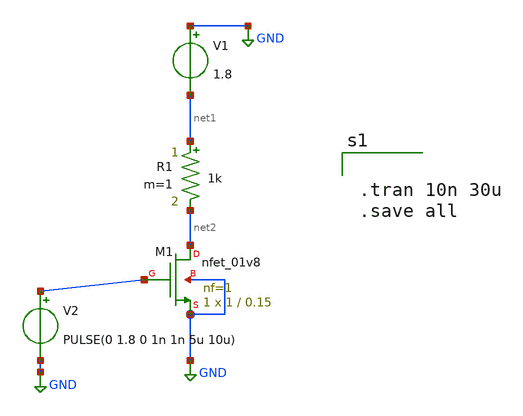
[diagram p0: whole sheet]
** sch_path: MOSFET_as_Switch/untitled.sch
**.subckt untitled
V1 GND net1 1.8
R1 net1 net2 1k m=1
V2 net3 GND PULSE(0 1.8 0 1n 1n 5u 10u)
XM1 net2 net3 GND GND sky130_fd_pr__nfet_01v8 L=0.15 W=1 nf=1 ad='int((1 + 1)/2) * 1 / 1 * 0.29' as='int((1 + 2)/2) * 1 / 1 * 0.29'
+ pd='2*int((1 + 1)/2) * (1 / 1 + 0.29)' ps='2*int((1 + 2)/2) * (1 / 1 + 0.29)' nrd='0.29 / 1 ' nrs='0.29 / 1 '
+ sa=0 sb=0 sd=0 mult=1 m=1
**** begin user architecture code


.tran 10n 30u
.save all


**** end user architecture code
**.ends
.GLOBAL GND
.end
